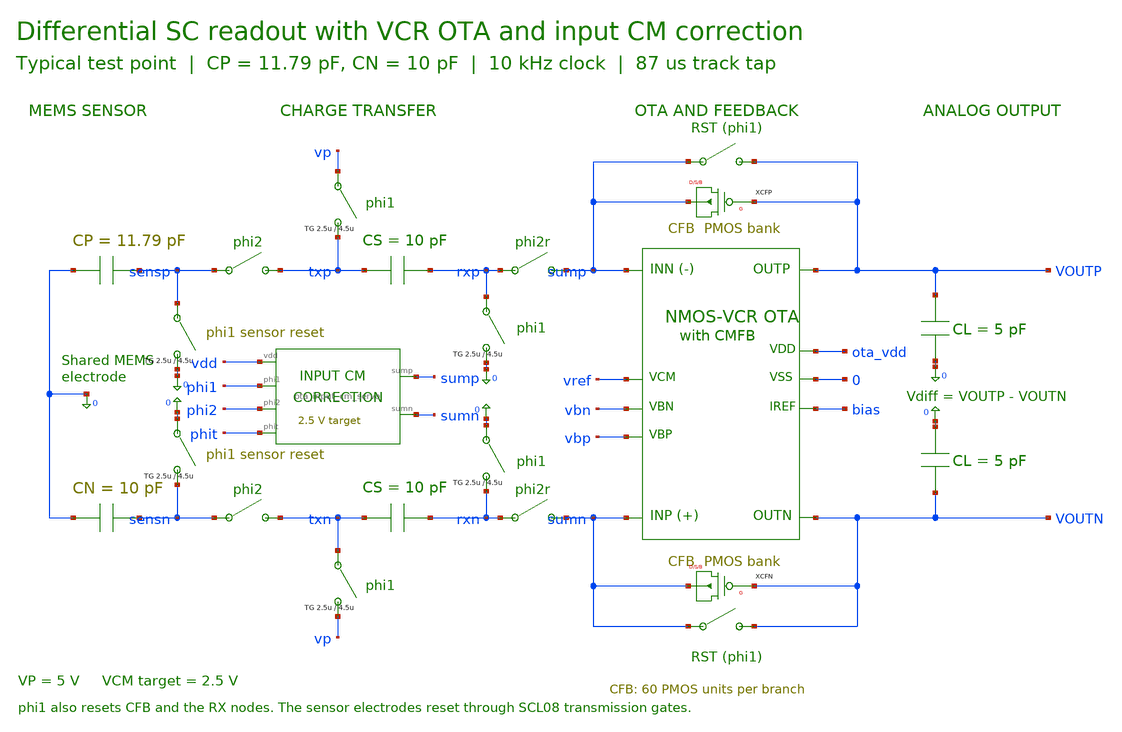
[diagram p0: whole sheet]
** sch_path: Fully_Integrated_Design/schematic/sc_vcr_input_cm.sch
**.subckt sc_vcr_input_cm
XOTA sumn sump outp outn ota_vdd 0 bias vref vbn vbp ota_telescopic_cm2p5
CMEMP 0 sensp 11.79p
XSENSEP sensp txp phi2 phi2b vdd 0 corrected_tg
XSRESETP phi1 0 sensp 0 vdd phi1b Transmission_v1_26
XCHARGEP phi1 0 vp txp vdd phi1b Transmission_v1_26
CSP txp rxp 10p
XRRESETP phi1 0 rxp 0 vdd phi1b Transmission_v1_26
XXFERP rxp sump phit phitb vdd 0 corrected_tg
XCFP sump outp sump sump P W=20u L=202.7u M=5 AD='( 20u ) * 4.5u' AS='( 20u ) * 4.5u' PD='2 * ( 20u ) + 9u'
+ PS='2 * ( 20u ) + 9u'
XFBRESETP sump outp phi1 phi1b vdd 0 corrected_tg
CLP outp 0 5p
CMEMN 0 sensn 10p
XSENSEN sensn txn phi2 phi2b vdd 0 corrected_tg
XSRESETN phi1 0 0 sensn vdd phi1b Transmission_v1_26
XCHARGEN phi1 0 txn vp vdd phi1b Transmission_v1_26
CSN txn rxn 10p
XRRESETN phi1 0 0 rxn vdd phi1b Transmission_v1_26
XXFERN rxn sumn phit phitb vdd 0 corrected_tg
XCFN sumn outn sumn sumn P W=20u L=202.7u M=5 AD='( 20u ) * 4.5u' AS='( 20u ) * 4.5u' PD='2 * ( 20u ) + 9u'
+ PS='2 * ( 20u ) + 9u'
XFBRESETN sumn outn phi1 phi1b vdd 0 corrected_tg
CLN 0 outn 5p
XICM sump sumn vdd phi1 phi2 phit ota_input_cm_servo
**** begin user architecture code
.include bench_support.spice
**** end user architecture code
**.ends

* expanding   symbol:  ota_input_cm_servo.sym # of pins=6
** sym_path: Mixed_Signal/Integrated_Design/symbols/ota_input_cm_servo.sym
** sch_path: Mixed_Signal/Integrated_Design/symbols/ota_input_cm_servo.sch
.subckt ota_input_cm_servo sump sumn vdd phi1 phi2 phit
*.iopin vdd
*.iopin phit
*.iopin phi1
*.iopin phi2
*.iopin sump
*.iopin sumn
BICMERR 0 cm_acc I = 1m*v(cm_sample)*(2.5-(v(sump)+v(sumn))/2)
CICMINT cm_acc 0 1n m=1
RICMINT cm_acc 0 1e13 m=1
VICMSAMPLE cm_sample 0 PULSE(0 1 84u 10n 10n 2u 100u)
BICMCTRL cm_ctrl 0 V = max(0,min(v(vdd),2.5+v(cm_acc)))
XSICMHOLD cm_ctrl cm_hold phi1 vdd user_tg_control
CICMHOLD cm_hold 0 20p m=1
RICMHOLD cm_hold cm_init 1e13 m=1
VICMINIT cm_init 0 2.5
XSICMEDGE1 vdd cm_edge1 phit vdd user_tg_control
XSICMRST1 0 cm_edge1 phi1 vdd user_tg_control
CICMEDGE1 cm_edge1 0 10p m=1
XSICMEDGE2 vdd cm_edge2 phi2 vdd user_tg_control
XSICMRST2 0 cm_edge2 phi1 vdd user_tg_control
CICMEDGE2 cm_edge2 0 10p m=1
BICMDRIVE cm_x 0 V = ((.68*v(cm_edge1)+.32*v(cm_edge2))/max(.1,v(vdd)))*v(cm_hold)
MCORRp sump cm_x sump sump P W=20u L=10u M=40 AD=90p AS=90p PD=49u PS=49u
MCORRn sumn cm_x sumn sumn P W=20u L=10u M=40 AD=90p AS=90p PD=49u PS=49u
**** begin user architecture code
.model icm_hold SW(Ron=10 Roff=1e14 Vt=2 Vh=.1)
.model icm_edge_set SW(Ron=3000 Roff=1e13 Vt=1 Vh=.05)
.model icm_edge_reset SW(Ron=100k Roff=1e13 Vt=2 Vh=.1)
**** end user architecture code
.ends

.end
